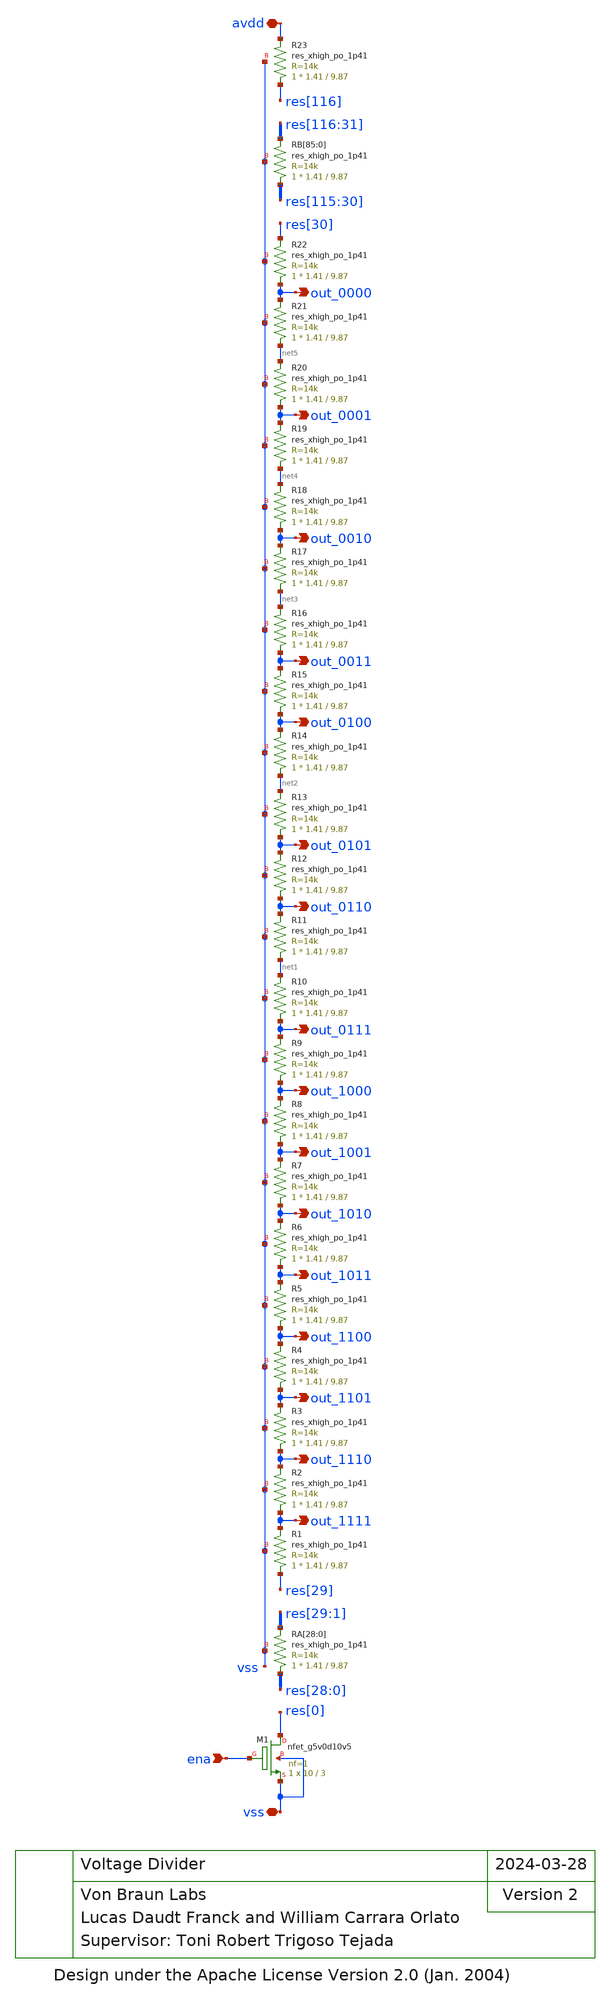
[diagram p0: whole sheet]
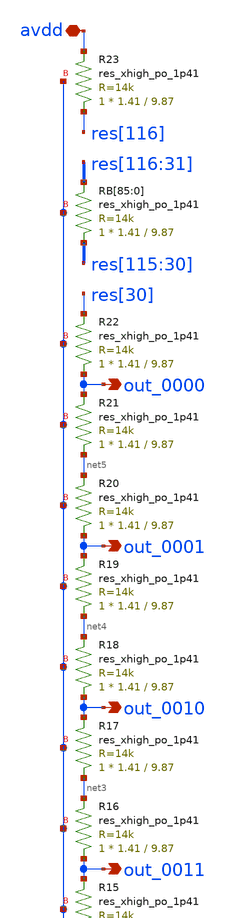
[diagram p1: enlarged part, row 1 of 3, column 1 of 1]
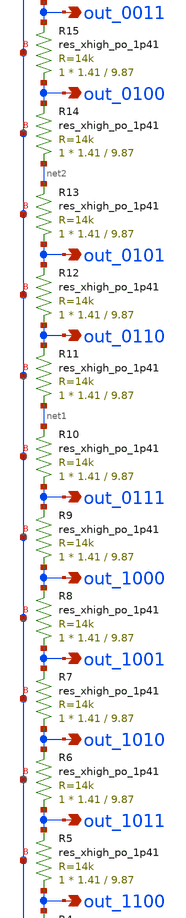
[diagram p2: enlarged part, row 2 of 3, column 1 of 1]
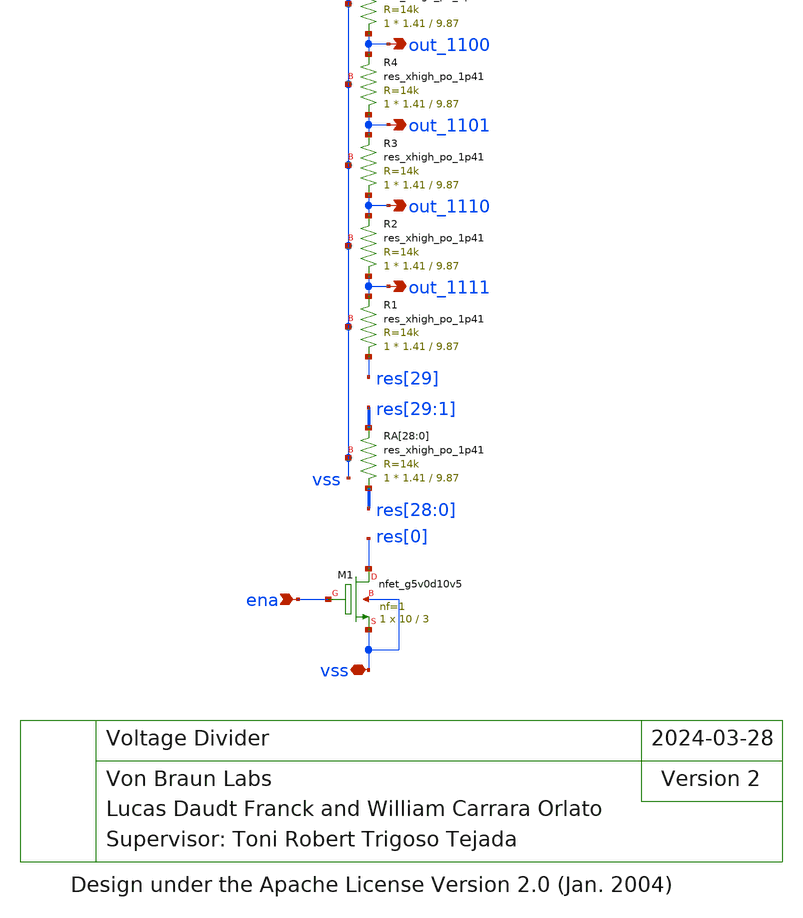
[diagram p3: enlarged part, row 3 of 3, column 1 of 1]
** sch_path: blocks/input/xschem/voltage_divider.sch
* Design under the Apache License Version 2.0 (Jan. 2004)
**.subckt voltage_divider ena vss avdd out_1111 out_1110 out_1101 out_1100 out_1011 out_1010
*+ out_1001 out_1000 out_0111 out_0110 out_0101 out_0100 out_0011 out_0010 out_0001 out_0000
*.ipin ena
*.iopin vss
*.iopin avdd
*.opin out_1111
*.opin out_1110
*.opin out_1101
*.opin out_1100
*.opin out_1011
*.opin out_1010
*.opin out_1001
*.opin out_1000
*.opin out_0111
*.opin out_0110
*.opin out_0101
*.opin out_0100
*.opin out_0011
*.opin out_0010
*.opin out_0001
*.opin out_0000
XM1 res[0] ena vss vss sky130_fd_pr__nfet_g5v0d10v5 L=3 W=10 nf=1 ad='int((nf+1)/2) * W/nf * 0.29' as='int((nf+2)/2) * W/nf * 0.29'
+ pd='2*int((nf+1)/2) * (W/nf + 0.29)' ps='2*int((nf+2)/2) * (W/nf + 0.29)' nrd='0.29 / W' nrs='0.29 / W'
+ sa=0 sb=0 sd=0 mult=1 m=1
XRA[28] res[28] res[29] vss sky130_fd_pr__res_xhigh_po_1p41 L=9.87 mult=1 m=1
XRA[27] res[27] res[28] vss sky130_fd_pr__res_xhigh_po_1p41 L=9.87 mult=1 m=1
XRA[26] res[26] res[27] vss sky130_fd_pr__res_xhigh_po_1p41 L=9.87 mult=1 m=1
XRA[25] res[25] res[26] vss sky130_fd_pr__res_xhigh_po_1p41 L=9.87 mult=1 m=1
XRA[24] res[24] res[25] vss sky130_fd_pr__res_xhigh_po_1p41 L=9.87 mult=1 m=1
XRA[23] res[23] res[24] vss sky130_fd_pr__res_xhigh_po_1p41 L=9.87 mult=1 m=1
XRA[22] res[22] res[23] vss sky130_fd_pr__res_xhigh_po_1p41 L=9.87 mult=1 m=1
XRA[21] res[21] res[22] vss sky130_fd_pr__res_xhigh_po_1p41 L=9.87 mult=1 m=1
XRA[20] res[20] res[21] vss sky130_fd_pr__res_xhigh_po_1p41 L=9.87 mult=1 m=1
XRA[19] res[19] res[20] vss sky130_fd_pr__res_xhigh_po_1p41 L=9.87 mult=1 m=1
XRA[18] res[18] res[19] vss sky130_fd_pr__res_xhigh_po_1p41 L=9.87 mult=1 m=1
XRA[17] res[17] res[18] vss sky130_fd_pr__res_xhigh_po_1p41 L=9.87 mult=1 m=1
XRA[16] res[16] res[17] vss sky130_fd_pr__res_xhigh_po_1p41 L=9.87 mult=1 m=1
XRA[15] res[15] res[16] vss sky130_fd_pr__res_xhigh_po_1p41 L=9.87 mult=1 m=1
XRA[14] res[14] res[15] vss sky130_fd_pr__res_xhigh_po_1p41 L=9.87 mult=1 m=1
XRA[13] res[13] res[14] vss sky130_fd_pr__res_xhigh_po_1p41 L=9.87 mult=1 m=1
XRA[12] res[12] res[13] vss sky130_fd_pr__res_xhigh_po_1p41 L=9.87 mult=1 m=1
XRA[11] res[11] res[12] vss sky130_fd_pr__res_xhigh_po_1p41 L=9.87 mult=1 m=1
XRA[10] res[10] res[11] vss sky130_fd_pr__res_xhigh_po_1p41 L=9.87 mult=1 m=1
XRA[9] res[9] res[10] vss sky130_fd_pr__res_xhigh_po_1p41 L=9.87 mult=1 m=1
XRA[8] res[8] res[9] vss sky130_fd_pr__res_xhigh_po_1p41 L=9.87 mult=1 m=1
XRA[7] res[7] res[8] vss sky130_fd_pr__res_xhigh_po_1p41 L=9.87 mult=1 m=1
XRA[6] res[6] res[7] vss sky130_fd_pr__res_xhigh_po_1p41 L=9.87 mult=1 m=1
XRA[5] res[5] res[6] vss sky130_fd_pr__res_xhigh_po_1p41 L=9.87 mult=1 m=1
XRA[4] res[4] res[5] vss sky130_fd_pr__res_xhigh_po_1p41 L=9.87 mult=1 m=1
XRA[3] res[3] res[4] vss sky130_fd_pr__res_xhigh_po_1p41 L=9.87 mult=1 m=1
XRA[2] res[2] res[3] vss sky130_fd_pr__res_xhigh_po_1p41 L=9.87 mult=1 m=1
XRA[1] res[1] res[2] vss sky130_fd_pr__res_xhigh_po_1p41 L=9.87 mult=1 m=1
XRA[0] res[0] res[1] vss sky130_fd_pr__res_xhigh_po_1p41 L=9.87 mult=1 m=1
XR1 res[29] out_1111 vss sky130_fd_pr__res_xhigh_po_1p41 L=9.87 mult=1 m=1
XR2 out_1111 out_1110 vss sky130_fd_pr__res_xhigh_po_1p41 L=9.87 mult=1 m=1
XR3 out_1110 out_1101 vss sky130_fd_pr__res_xhigh_po_1p41 L=9.87 mult=1 m=1
XR4 out_1101 out_1100 vss sky130_fd_pr__res_xhigh_po_1p41 L=9.87 mult=1 m=1
XR5 out_1100 out_1011 vss sky130_fd_pr__res_xhigh_po_1p41 L=9.87 mult=1 m=1
XR6 out_1011 out_1010 vss sky130_fd_pr__res_xhigh_po_1p41 L=9.87 mult=1 m=1
XR7 out_1010 out_1001 vss sky130_fd_pr__res_xhigh_po_1p41 L=9.87 mult=1 m=1
XR8 out_1001 out_1000 vss sky130_fd_pr__res_xhigh_po_1p41 L=9.87 mult=1 m=1
XR9 out_1000 out_0111 vss sky130_fd_pr__res_xhigh_po_1p41 L=9.87 mult=1 m=1
XR10 out_0111 net1 vss sky130_fd_pr__res_xhigh_po_1p41 L=9.87 mult=1 m=1
XR11 net1 out_0110 vss sky130_fd_pr__res_xhigh_po_1p41 L=9.87 mult=1 m=1
XR12 out_0110 out_0101 vss sky130_fd_pr__res_xhigh_po_1p41 L=9.87 mult=1 m=1
XR13 out_0101 net2 vss sky130_fd_pr__res_xhigh_po_1p41 L=9.87 mult=1 m=1
XR14 net2 out_0100 vss sky130_fd_pr__res_xhigh_po_1p41 L=9.87 mult=1 m=1
XR15 out_0100 out_0011 vss sky130_fd_pr__res_xhigh_po_1p41 L=9.87 mult=1 m=1
XR16 out_0011 net3 vss sky130_fd_pr__res_xhigh_po_1p41 L=9.87 mult=1 m=1
XR17 net3 out_0010 vss sky130_fd_pr__res_xhigh_po_1p41 L=9.87 mult=1 m=1
XR18 out_0010 net4 vss sky130_fd_pr__res_xhigh_po_1p41 L=9.87 mult=1 m=1
XR19 net4 out_0001 vss sky130_fd_pr__res_xhigh_po_1p41 L=9.87 mult=1 m=1
XR20 out_0001 net5 vss sky130_fd_pr__res_xhigh_po_1p41 L=9.87 mult=1 m=1
XR21 net5 out_0000 vss sky130_fd_pr__res_xhigh_po_1p41 L=9.87 mult=1 m=1
XR22 out_0000 res[30] vss sky130_fd_pr__res_xhigh_po_1p41 L=9.87 mult=1 m=1
XRB[85] res[115] res[116] vss sky130_fd_pr__res_xhigh_po_1p41 L=9.87 mult=1 m=1
XRB[84] res[114] res[115] vss sky130_fd_pr__res_xhigh_po_1p41 L=9.87 mult=1 m=1
XRB[83] res[113] res[114] vss sky130_fd_pr__res_xhigh_po_1p41 L=9.87 mult=1 m=1
XRB[82] res[112] res[113] vss sky130_fd_pr__res_xhigh_po_1p41 L=9.87 mult=1 m=1
XRB[81] res[111] res[112] vss sky130_fd_pr__res_xhigh_po_1p41 L=9.87 mult=1 m=1
XRB[80] res[110] res[111] vss sky130_fd_pr__res_xhigh_po_1p41 L=9.87 mult=1 m=1
XRB[79] res[109] res[110] vss sky130_fd_pr__res_xhigh_po_1p41 L=9.87 mult=1 m=1
XRB[78] res[108] res[109] vss sky130_fd_pr__res_xhigh_po_1p41 L=9.87 mult=1 m=1
XRB[77] res[107] res[108] vss sky130_fd_pr__res_xhigh_po_1p41 L=9.87 mult=1 m=1
XRB[76] res[106] res[107] vss sky130_fd_pr__res_xhigh_po_1p41 L=9.87 mult=1 m=1
XRB[75] res[105] res[106] vss sky130_fd_pr__res_xhigh_po_1p41 L=9.87 mult=1 m=1
XRB[74] res[104] res[105] vss sky130_fd_pr__res_xhigh_po_1p41 L=9.87 mult=1 m=1
XRB[73] res[103] res[104] vss sky130_fd_pr__res_xhigh_po_1p41 L=9.87 mult=1 m=1
XRB[72] res[102] res[103] vss sky130_fd_pr__res_xhigh_po_1p41 L=9.87 mult=1 m=1
XRB[71] res[101] res[102] vss sky130_fd_pr__res_xhigh_po_1p41 L=9.87 mult=1 m=1
XRB[70] res[100] res[101] vss sky130_fd_pr__res_xhigh_po_1p41 L=9.87 mult=1 m=1
XRB[69] res[99] res[100] vss sky130_fd_pr__res_xhigh_po_1p41 L=9.87 mult=1 m=1
XRB[68] res[98] res[99] vss sky130_fd_pr__res_xhigh_po_1p41 L=9.87 mult=1 m=1
XRB[67] res[97] res[98] vss sky130_fd_pr__res_xhigh_po_1p41 L=9.87 mult=1 m=1
XRB[66] res[96] res[97] vss sky130_fd_pr__res_xhigh_po_1p41 L=9.87 mult=1 m=1
XRB[65] res[95] res[96] vss sky130_fd_pr__res_xhigh_po_1p41 L=9.87 mult=1 m=1
XRB[64] res[94] res[95] vss sky130_fd_pr__res_xhigh_po_1p41 L=9.87 mult=1 m=1
XRB[63] res[93] res[94] vss sky130_fd_pr__res_xhigh_po_1p41 L=9.87 mult=1 m=1
XRB[62] res[92] res[93] vss sky130_fd_pr__res_xhigh_po_1p41 L=9.87 mult=1 m=1
XRB[61] res[91] res[92] vss sky130_fd_pr__res_xhigh_po_1p41 L=9.87 mult=1 m=1
XRB[60] res[90] res[91] vss sky130_fd_pr__res_xhigh_po_1p41 L=9.87 mult=1 m=1
XRB[59] res[89] res[90] vss sky130_fd_pr__res_xhigh_po_1p41 L=9.87 mult=1 m=1
XRB[58] res[88] res[89] vss sky130_fd_pr__res_xhigh_po_1p41 L=9.87 mult=1 m=1
XRB[57] res[87] res[88] vss sky130_fd_pr__res_xhigh_po_1p41 L=9.87 mult=1 m=1
XRB[56] res[86] res[87] vss sky130_fd_pr__res_xhigh_po_1p41 L=9.87 mult=1 m=1
XRB[55] res[85] res[86] vss sky130_fd_pr__res_xhigh_po_1p41 L=9.87 mult=1 m=1
XRB[54] res[84] res[85] vss sky130_fd_pr__res_xhigh_po_1p41 L=9.87 mult=1 m=1
XRB[53] res[83] res[84] vss sky130_fd_pr__res_xhigh_po_1p41 L=9.87 mult=1 m=1
XRB[52] res[82] res[83] vss sky130_fd_pr__res_xhigh_po_1p41 L=9.87 mult=1 m=1
XRB[51] res[81] res[82] vss sky130_fd_pr__res_xhigh_po_1p41 L=9.87 mult=1 m=1
XRB[50] res[80] res[81] vss sky130_fd_pr__res_xhigh_po_1p41 L=9.87 mult=1 m=1
XRB[49] res[79] res[80] vss sky130_fd_pr__res_xhigh_po_1p41 L=9.87 mult=1 m=1
XRB[48] res[78] res[79] vss sky130_fd_pr__res_xhigh_po_1p41 L=9.87 mult=1 m=1
XRB[47] res[77] res[78] vss sky130_fd_pr__res_xhigh_po_1p41 L=9.87 mult=1 m=1
XRB[46] res[76] res[77] vss sky130_fd_pr__res_xhigh_po_1p41 L=9.87 mult=1 m=1
XRB[45] res[75] res[76] vss sky130_fd_pr__res_xhigh_po_1p41 L=9.87 mult=1 m=1
XRB[44] res[74] res[75] vss sky130_fd_pr__res_xhigh_po_1p41 L=9.87 mult=1 m=1
XRB[43] res[73] res[74] vss sky130_fd_pr__res_xhigh_po_1p41 L=9.87 mult=1 m=1
XRB[42] res[72] res[73] vss sky130_fd_pr__res_xhigh_po_1p41 L=9.87 mult=1 m=1
XRB[41] res[71] res[72] vss sky130_fd_pr__res_xhigh_po_1p41 L=9.87 mult=1 m=1
XRB[40] res[70] res[71] vss sky130_fd_pr__res_xhigh_po_1p41 L=9.87 mult=1 m=1
XRB[39] res[69] res[70] vss sky130_fd_pr__res_xhigh_po_1p41 L=9.87 mult=1 m=1
XRB[38] res[68] res[69] vss sky130_fd_pr__res_xhigh_po_1p41 L=9.87 mult=1 m=1
XRB[37] res[67] res[68] vss sky130_fd_pr__res_xhigh_po_1p41 L=9.87 mult=1 m=1
XRB[36] res[66] res[67] vss sky130_fd_pr__res_xhigh_po_1p41 L=9.87 mult=1 m=1
XRB[35] res[65] res[66] vss sky130_fd_pr__res_xhigh_po_1p41 L=9.87 mult=1 m=1
XRB[34] res[64] res[65] vss sky130_fd_pr__res_xhigh_po_1p41 L=9.87 mult=1 m=1
XRB[33] res[63] res[64] vss sky130_fd_pr__res_xhigh_po_1p41 L=9.87 mult=1 m=1
XRB[32] res[62] res[63] vss sky130_fd_pr__res_xhigh_po_1p41 L=9.87 mult=1 m=1
XRB[31] res[61] res[62] vss sky130_fd_pr__res_xhigh_po_1p41 L=9.87 mult=1 m=1
XRB[30] res[60] res[61] vss sky130_fd_pr__res_xhigh_po_1p41 L=9.87 mult=1 m=1
XRB[29] res[59] res[60] vss sky130_fd_pr__res_xhigh_po_1p41 L=9.87 mult=1 m=1
XRB[28] res[58] res[59] vss sky130_fd_pr__res_xhigh_po_1p41 L=9.87 mult=1 m=1
XRB[27] res[57] res[58] vss sky130_fd_pr__res_xhigh_po_1p41 L=9.87 mult=1 m=1
XRB[26] res[56] res[57] vss sky130_fd_pr__res_xhigh_po_1p41 L=9.87 mult=1 m=1
XRB[25] res[55] res[56] vss sky130_fd_pr__res_xhigh_po_1p41 L=9.87 mult=1 m=1
XRB[24] res[54] res[55] vss sky130_fd_pr__res_xhigh_po_1p41 L=9.87 mult=1 m=1
XRB[23] res[53] res[54] vss sky130_fd_pr__res_xhigh_po_1p41 L=9.87 mult=1 m=1
XRB[22] res[52] res[53] vss sky130_fd_pr__res_xhigh_po_1p41 L=9.87 mult=1 m=1
XRB[21] res[51] res[52] vss sky130_fd_pr__res_xhigh_po_1p41 L=9.87 mult=1 m=1
XRB[20] res[50] res[51] vss sky130_fd_pr__res_xhigh_po_1p41 L=9.87 mult=1 m=1
XRB[19] res[49] res[50] vss sky130_fd_pr__res_xhigh_po_1p41 L=9.87 mult=1 m=1
XRB[18] res[48] res[49] vss sky130_fd_pr__res_xhigh_po_1p41 L=9.87 mult=1 m=1
XRB[17] res[47] res[48] vss sky130_fd_pr__res_xhigh_po_1p41 L=9.87 mult=1 m=1
XRB[16] res[46] res[47] vss sky130_fd_pr__res_xhigh_po_1p41 L=9.87 mult=1 m=1
XRB[15] res[45] res[46] vss sky130_fd_pr__res_xhigh_po_1p41 L=9.87 mult=1 m=1
XRB[14] res[44] res[45] vss sky130_fd_pr__res_xhigh_po_1p41 L=9.87 mult=1 m=1
XRB[13] res[43] res[44] vss sky130_fd_pr__res_xhigh_po_1p41 L=9.87 mult=1 m=1
XRB[12] res[42] res[43] vss sky130_fd_pr__res_xhigh_po_1p41 L=9.87 mult=1 m=1
XRB[11] res[41] res[42] vss sky130_fd_pr__res_xhigh_po_1p41 L=9.87 mult=1 m=1
XRB[10] res[40] res[41] vss sky130_fd_pr__res_xhigh_po_1p41 L=9.87 mult=1 m=1
XRB[9] res[39] res[40] vss sky130_fd_pr__res_xhigh_po_1p41 L=9.87 mult=1 m=1
XRB[8] res[38] res[39] vss sky130_fd_pr__res_xhigh_po_1p41 L=9.87 mult=1 m=1
XRB[7] res[37] res[38] vss sky130_fd_pr__res_xhigh_po_1p41 L=9.87 mult=1 m=1
XRB[6] res[36] res[37] vss sky130_fd_pr__res_xhigh_po_1p41 L=9.87 mult=1 m=1
XRB[5] res[35] res[36] vss sky130_fd_pr__res_xhigh_po_1p41 L=9.87 mult=1 m=1
XRB[4] res[34] res[35] vss sky130_fd_pr__res_xhigh_po_1p41 L=9.87 mult=1 m=1
XRB[3] res[33] res[34] vss sky130_fd_pr__res_xhigh_po_1p41 L=9.87 mult=1 m=1
XRB[2] res[32] res[33] vss sky130_fd_pr__res_xhigh_po_1p41 L=9.87 mult=1 m=1
XRB[1] res[31] res[32] vss sky130_fd_pr__res_xhigh_po_1p41 L=9.87 mult=1 m=1
XRB[0] res[30] res[31] vss sky130_fd_pr__res_xhigh_po_1p41 L=9.87 mult=1 m=1
XR23 res[116] avdd vss sky130_fd_pr__res_xhigh_po_1p41 L=9.87 mult=1 m=1
**.ends
.end
